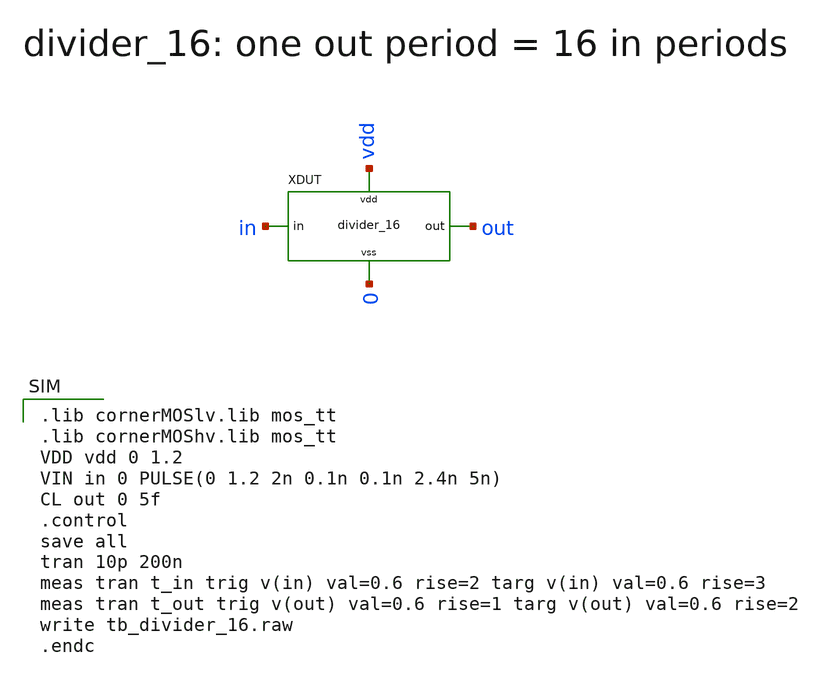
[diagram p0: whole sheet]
** sch_path: verification/tb_divider_16.sch
**.subckt tb_divider_16
XDUT in out vdd 0 divider_16
**** begin user architecture code

.lib cornerMOSlv.lib mos_tt
.lib cornerMOShv.lib mos_tt
VDD vdd 0 1.2
VIN in 0 PULSE(0 1.2 2n 0.1n 0.1n 2.4n 5n)
CL out 0 5f
.control
save all
tran 10p 200n
meas tran t_in trig v(in) val=0.6 rise=2 targ v(in) val=0.6 rise=3
meas tran t_out trig v(out) val=0.6 rise=1 targ v(out) val=0.6 rise=2
write tb_divider_16.raw
.endc

**** end user architecture code
**.ends

* expanding   symbol:  schematics/divider_16.sym # of pins=4
** sym_path: xschem/schematics/divider_16.sym
** sch_path: xschem/schematics/divider_16.sch
.subckt divider_16 in out vdd vss
*.iopin in
*.iopin out
*.iopin vdd
*.iopin vss
XB1 net1 in vdd vss sg13cmos5l_inv_1
XB2 net2 net1 vdd vss sg13cmos5l_inv_1
X1 net3 net2 net4 net3 vdd vss dff_c2mos
X2 net5 net4 net6 net5 vdd vss dff_c2mos
X3 net7 net6 net8 net7 vdd vss dff_c2mos
X4 net9 net8 out net9 vdd vss dff_c2mos
.ends


* expanding   symbol:  logic_gates/sg13cmos5l_inv_1.sym # of pins=4
** sym_path: xschem/logic_gates/sg13cmos5l_inv_1.sym
** sch_path: xschem/logic_gates/sg13cmos5l_inv_1.sch
.subckt sg13cmos5l_inv_1 Y A VDD VSS
*.iopin Y
*.iopin A
*.iopin VDD
*.iopin VSS
XMN0 Y A VSS VSS sg13_lv_nmos w=0.74u l=0.13u ng=1 m=1
XMP0 VDD A Y VDD sg13_lv_pmos w=1.12u l=0.13u ng=1 m=1
.ends


* expanding   symbol:  schematics/dff_c2mos.sym # of pins=6
** sym_path: xschem/schematics/dff_c2mos.sym
** sch_path: xschem/schematics/dff_c2mos.sch
.subckt dff_c2mos d clk q qb vdd vss
*.iopin d
*.iopin q
*.iopin qb
*.iopin clk
*.iopin vdd
*.iopin vss
XMT1N net1 clkb d vss sg13_lv_nmos w=0.6u l=0.13u ng=1 m=1
XMT1P d clki net1 vdd sg13_lv_pmos w=1.2u l=0.13u ng=1 m=1
XMT3N net3 clki net2 vss sg13_lv_nmos w=0.6u l=0.13u ng=1 m=1
XMT3P net2 clkb net3 vdd sg13_lv_pmos w=1.2u l=0.13u ng=1 m=1
XMT2P net4 clkb net1 vdd sg13_lv_pmos w=0.6u l=0.13u ng=1 m=1
XMT2N net1 clki net4 vss sg13_lv_nmos w=0.3u l=0.13u ng=1 m=1
XMT4P net5 clki net3 vdd sg13_lv_pmos w=0.6u l=0.13u ng=1 m=1
XMT4N net3 clkb net5 vss sg13_lv_nmos w=0.3u l=0.13u ng=1 m=1
XI1 net2 net1 vdd vss sg13cmos5l_inv_1
XI3 net6 net3 vdd vss sg13cmos5l_inv_1
XI5 qb net6 vdd vss sg13cmos5l_inv_1
XI6 q qb vdd vss sg13cmos5l_inv_1
XI2 net2 net4 vdd vss INVLVW
XI4 net6 net5 vdd vss INVLVW
XI0 clkb clk vdd vss sg13cmos5l_inv_1
XI9 clki clkb vdd vss sg13cmos5l_inv_1
.ends


* expanding   symbol:  logic_gates/INVLVW.sym # of pins=4
** sym_path: xschem/logic_gates/INVLVW.sym
** sch_path: xschem/logic_gates/INVLVW.sch
.subckt INVLVW a y vdd vss
*.iopin vdd
*.iopin vss
*.iopin y
*.iopin a
XMP vdd a y vdd sg13_lv_pmos w=0.3u l=0.3u ng=1 m=1
XMN y a vss vss sg13_lv_nmos w=0.3u l=0.3u ng=1 m=1
.ends

.end
